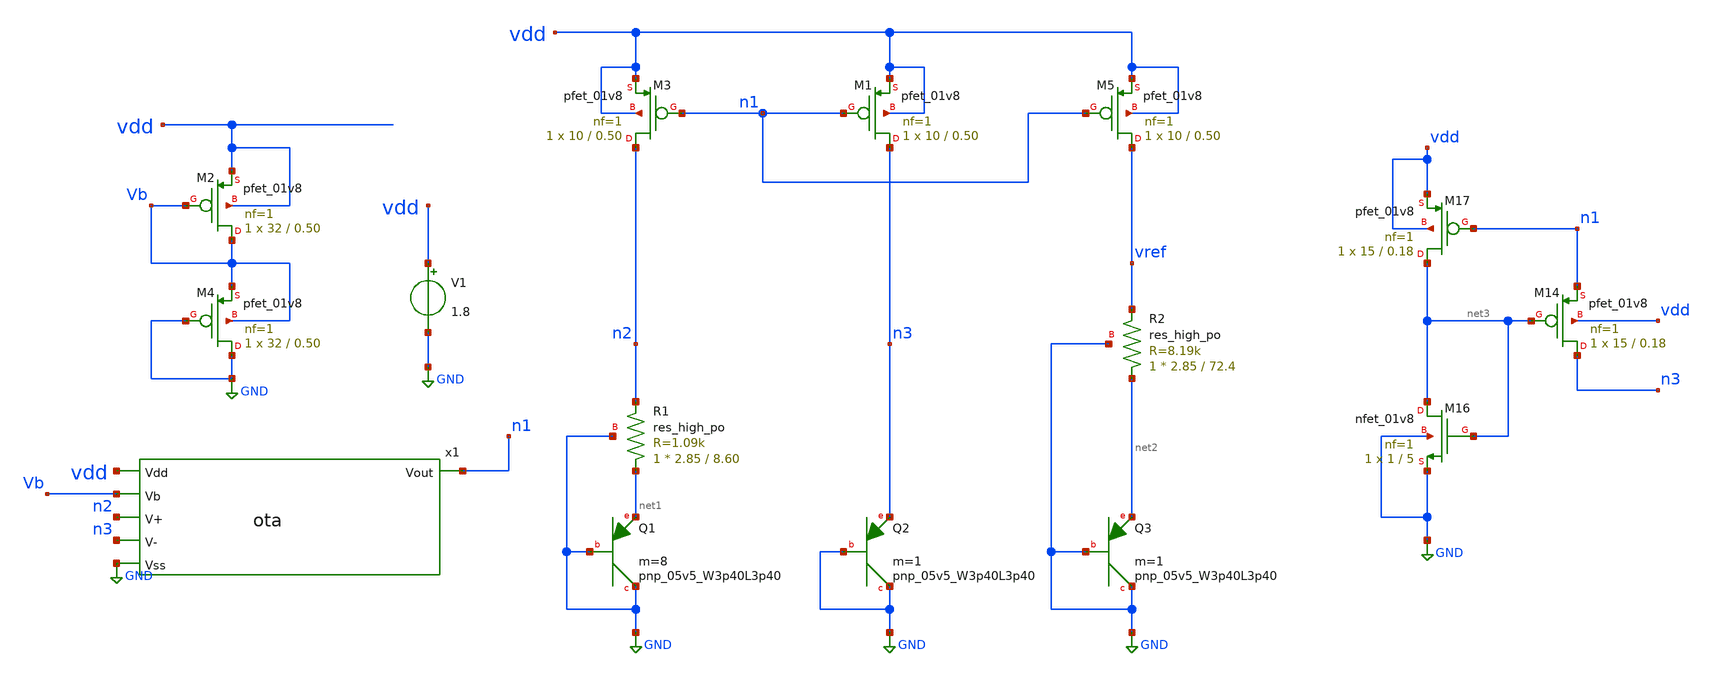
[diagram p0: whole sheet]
** sch_path: Bandgap/Bandgap.sch
**.subckt Bandgap
V1 vdd GND 1.8
XM1 n3 n1 vdd vdd sky130_fd_pr__pfet_01v8 L=0.50 W=10 nf=1 ad='int((1 + 1)/2) * 10 / 1 * 0.29' as='int((1 + 2)/2) * 10 / 1 * 0.29'
+ pd='2*int((1 + 1)/2) * (10 / 1 + 0.29)' ps='2*int((1 + 2)/2) * (10 / 1 + 0.29)' nrd='0.29 / 10 ' nrs='0.29 / 10 '
+ sa=0 sb=0 sd=0 mult=1 m=1
XM3 n2 n1 vdd vdd sky130_fd_pr__pfet_01v8 L=0.50 W=10 nf=1 ad='int((1 + 1)/2) * 10 / 1 * 0.29' as='int((1 + 2)/2) * 10 / 1 * 0.29'
+ pd='2*int((1 + 1)/2) * (10 / 1 + 0.29)' ps='2*int((1 + 2)/2) * (10 / 1 + 0.29)' nrd='0.29 / 10 ' nrs='0.29 / 10 '
+ sa=0 sb=0 sd=0 mult=1 m=1
XQ1 GND GND net1 sky130_fd_pr__pnp_05v5_W3p40L3p40 m=8
XQ2 GND GND n3 sky130_fd_pr__pnp_05v5_W3p40L3p40 m=1
XM2 Vb Vb vdd vdd sky130_fd_pr__pfet_01v8 L=0.50 W=32 nf=1 ad='int((1 + 1)/2) * 32 / 1 * 0.29' as='int((1 + 2)/2) * 32 / 1 * 0.29'
+ pd='2*int((1 + 1)/2) * (32 / 1 + 0.29)' ps='2*int((1 + 2)/2) * (32 / 1 + 0.29)' nrd='0.29 / 32 ' nrs='0.29 / 32 '
+ sa=0 sb=0 sd=0 mult=1 m=1
XM4 GND GND Vb Vb sky130_fd_pr__pfet_01v8 L=0.50 W=32 nf=1 ad='int((1 + 1)/2) * 32 / 1 * 0.29' as='int((1 + 2)/2) * 32 / 1 * 0.29'
+ pd='2*int((1 + 1)/2) * (32 / 1 + 0.29)' ps='2*int((1 + 2)/2) * (32 / 1 + 0.29)' nrd='0.29 / 32 ' nrs='0.29 / 32 '
+ sa=0 sb=0 sd=0 mult=1 m=1
XM5 vref n1 vdd vdd sky130_fd_pr__pfet_01v8 L=0.50 W=10 nf=1 ad='int((1 + 1)/2) * 10 / 1 * 0.29' as='int((1 + 2)/2) * 10 / 1 * 0.29'
+ pd='2*int((1 + 1)/2) * (10 / 1 + 0.29)' ps='2*int((1 + 2)/2) * (10 / 1 + 0.29)' nrd='0.29 / 10 ' nrs='0.29 / 10 '
+ sa=0 sb=0 sd=0 mult=1 m=1
XQ3 GND GND net2 sky130_fd_pr__pnp_05v5_W3p40L3p40 m=1
x1 vdd Vb n2 n3 n1 GND ota
XR1 net1 n2 GND sky130_fd_pr__res_high_po W=2.85 L=8.60 mult=1 m=1
XR2 net2 vref GND sky130_fd_pr__res_high_po W=2.85 L=72.4 mult=1 m=1
XM14 n3 net3 n1 vdd sky130_fd_pr__pfet_01v8 L=0.18 W=15 nf=1 ad='int((1 + 1)/2) * 15 / 1 * 0.29' as='int((1 + 2)/2) * 15 / 1 * 0.29'
+ pd='2*int((1 + 1)/2) * (15 / 1 + 0.29)' ps='2*int((1 + 2)/2) * (15 / 1 + 0.29)' nrd='0.29 / 15 ' nrs='0.29 / 15 '
+ sa=0 sb=0 sd=0 mult=1 m=1
XM16 net3 net3 GND GND sky130_fd_pr__nfet_01v8 L=5 W=1 nf=1 ad='int((1 + 1)/2) * 1 / 1 * 0.29' as='int((1 + 2)/2) * 1 / 1 * 0.29'
+ pd='2*int((1 + 1)/2) * (1 / 1 + 0.29)' ps='2*int((1 + 2)/2) * (1 / 1 + 0.29)' nrd='0.29 / 1 ' nrs='0.29 / 1 '
+ sa=0 sb=0 sd=0 mult=1 m=1
XM17 net3 n1 vdd vdd sky130_fd_pr__pfet_01v8 L=0.18 W=15 nf=1 ad='int((1 + 1)/2) * 15 / 1 * 0.29' as='int((1 + 2)/2) * 15 / 1 * 0.29'
+ pd='2*int((1 + 1)/2) * (15 / 1 + 0.29)' ps='2*int((1 + 2)/2) * (15 / 1 + 0.29)' nrd='0.29 / 15 ' nrs='0.29 / 15 '
+ sa=0 sb=0 sd=0 mult=1 m=1
**** begin user architecture code


.save all
.options savecurrent
.control
  dc temp -40 120 0.1
  write tt.raw vref
  quit
.endc


.lib $::SKYWATER_MODELS/sky130.lib.spice tt
**** end user architecture code
**.ends

* expanding   symbol:  ota.sym # of pins=6
** sym_path: Bandgap/ota.sym
** sch_path: Bandgap/ota.sch
.subckt ota Vdd Vb V+ V- Vout Vss
*.ipin Vdd
*.opin Vout
*.ipin V+
*.ipin V-
*.ipin Vss
*.ipin Vb
XM1 net1 Vb Vdd Vdd sky130_fd_pr__pfet_01v8 L=0.50 W=16 nf=1 ad='int((1 + 1)/2) * 16 / 1 * 0.29' as='int((1 + 2)/2) * 16 / 1 * 0.29'
+ pd='2*int((1 + 1)/2) * (16 / 1 + 0.29)' ps='2*int((1 + 2)/2) * (16 / 1 + 0.29)' nrd='0.29 / 16 ' nrs='0.29 / 16 '
+ sa=0 sb=0 sd=0 mult=1 m=1
XM2 net2 V+ net1 net1 sky130_fd_pr__pfet_01v8 L=0.50 W=16 nf=1 ad='int((1 + 1)/2) * 16 / 1 * 0.29' as='int((1 + 2)/2) * 16 / 1 * 0.29'
+ pd='2*int((1 + 1)/2) * (16 / 1 + 0.29)' ps='2*int((1 + 2)/2) * (16 / 1 + 0.29)' nrd='0.29 / 16 ' nrs='0.29 / 16 '
+ sa=0 sb=0 sd=0 mult=1 m=1
XM3 Vout V- net1 net1 sky130_fd_pr__pfet_01v8 L=0.50 W=16 nf=1 ad='int((1 + 1)/2) * 16 / 1 * 0.29' as='int((1 + 2)/2) * 16 / 1 * 0.29'
+ pd='2*int((1 + 1)/2) * (16 / 1 + 0.29)' ps='2*int((1 + 2)/2) * (16 / 1 + 0.29)' nrd='0.29 / 16 ' nrs='0.29 / 16 '
+ sa=0 sb=0 sd=0 mult=1 m=1
XM4 Vout net2 Vss Vss sky130_fd_pr__nfet_01v8 L=1 W=10 nf=1 ad='int((1 + 1)/2) * 10 / 1 * 0.29' as='int((1 + 2)/2) * 10 / 1 * 0.29'
+ pd='2*int((1 + 1)/2) * (10 / 1 + 0.29)' ps='2*int((1 + 2)/2) * (10 / 1 + 0.29)' nrd='0.29 / 10 ' nrs='0.29 / 10 '
+ sa=0 sb=0 sd=0 mult=1 m=1
XM5 net2 net2 Vss Vss sky130_fd_pr__nfet_01v8 L=1 W=10 nf=1 ad='int((1 + 1)/2) * 10 / 1 * 0.29' as='int((1 + 2)/2) * 10 / 1 * 0.29'
+ pd='2*int((1 + 1)/2) * (10 / 1 + 0.29)' ps='2*int((1 + 2)/2) * (10 / 1 + 0.29)' nrd='0.29 / 10 ' nrs='0.29 / 10 '
+ sa=0 sb=0 sd=0 mult=1 m=1
.ends

.GLOBAL GND
.end
